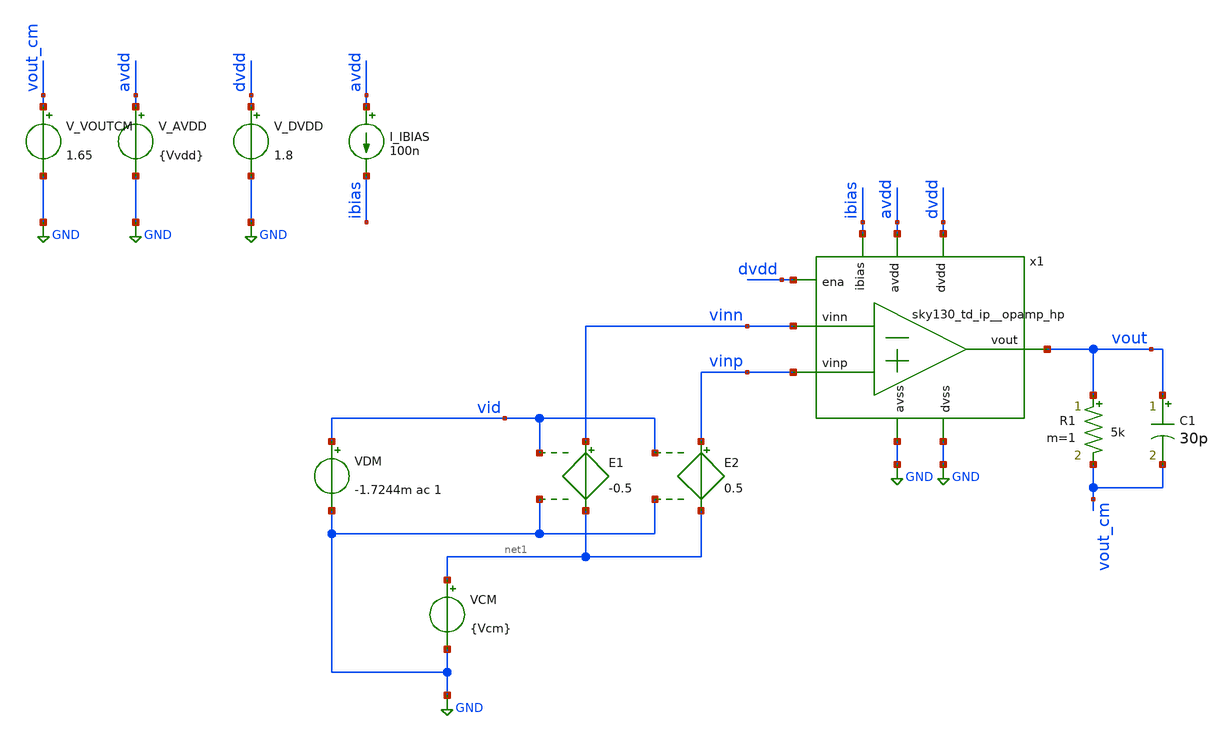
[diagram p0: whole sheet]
** sch_path: cace/gbw.sch
**.subckt gbw
x1 avdd vout ibias vinn vinp GND dvdd GND dvdd sky130_td_ip__opamp_hp
V_AVDD avdd GND {Vvdd}
.save i(v_avdd)
V_DVDD dvdd GND 1.8
.save i(v_dvdd)
I_IBIAS avdd ibias 100n
VCM net1 GND {Vcm}
R1 vout vout_cm 5k m=1
C1 vout vout_cm 30p m=1
V_VOUTCM vout_cm GND 1.65
.save i(v_voutcm)
E1 vinn net1 vid GND -0.5
VDM vid GND -1.7244m ac 1
E2 vinp net1 vid GND 0.5
**** begin user architecture code


.control
save all

* Calculate input offset voltage
alter @VDM[pwl] = [ 0 -10m 10 10m ]
tran 1m 10
run
let vid = v(vid)
let vout = v(vout)
meas tran input_offset_voltage FIND vid WHEN vout=1.65 RISE=LAST


alter @VDM[pwl] = [ 0 0 ]
alter VDM dc = $&input_offset_voltage
alter VDM ac = 1

* Run AC sweep from 1Hz to 1GHz
AC DEC 100 1 1000000000
run

* Get DC gain in DBs.
let av_db = db(vout / vid)
let av_lin = mag(vout / vid)
let ol_phase = 180/PI*phase(vout / vid)

meas AC av0_db FIND av_db AT=1
meas AC av0_lin FIND av_lin AT=1
let av0_minus_3 = av0_db - 3
meas AC fp1 WHEN av_db=av0_minus_3
meas AC ugf WHEN av_db=0
meas AC ol_phase_at_ugf FIND ol_phase AT=ugf

let pm = 180 + ol_phase_at_ugf
let gbw = av0_lin * fp1

echo
echo ===================================
echo Open-Loop characterization results:
echo - DC Gain: $&av0_db
echo - 3-dB frequency: $&fp1
echo - GBW: $&gbw
echo - PM: $&pm
echo ===================================

echo $&av0_db $&gbw $&pm > {simpath}/{filename}_{N}.data
quit
.endc




* CACE gensim simulation file {filename}_{N}
* Generated by CACE gensim, Efabless Corporation (c) 2023
* Find the power supply rejection ratio of the amplifier

.include {DUT_path}

.lib {PDK_ROOT}/{PDK}/libs.tech/combined/sky130.lib.spice {corner}

.option TEMP={temperature}
* Flag unsafe operating conditions (exceeds models' specified limits)
.option warn=1
.option SEED=[{seed=12345} + {iterations=0}]


**** end user architecture code
**.ends
.GLOBAL GND
.end
